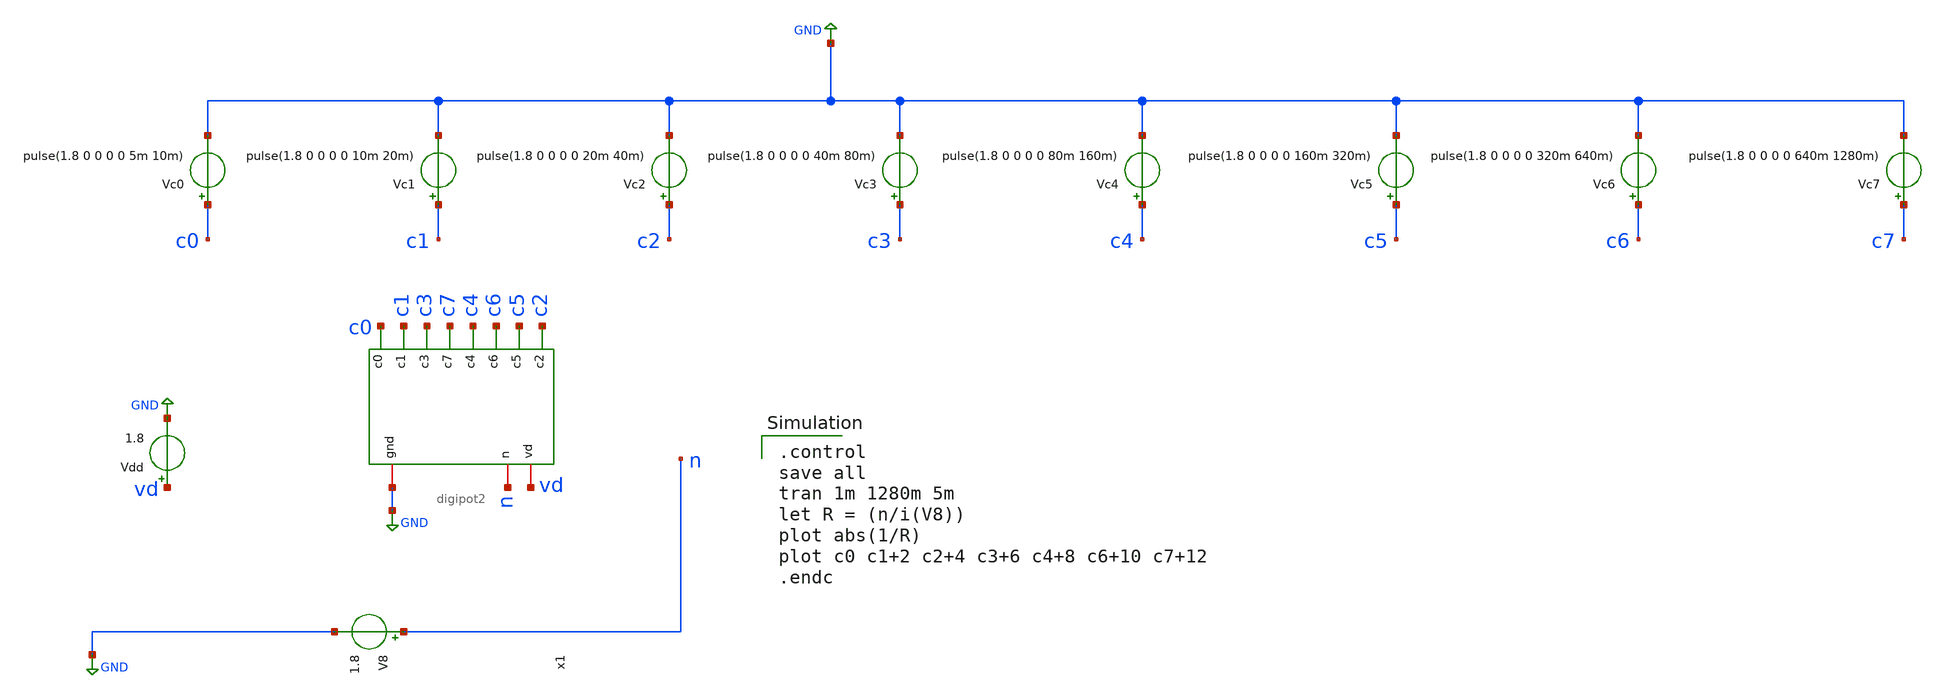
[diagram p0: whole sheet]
** sch_path: .Trash-1000/files/dp2tb.sch
**.subckt dp2tb
V8 n GND 1.8
Vdd vd GND 1.8
Vc0 c0 GND pulse(1.8 0 0 0 0 5m 10m)
Vc1 c1 GND pulse(1.8 0 0 0 0 10m 20m)
Vc2 c2 GND pulse(1.8 0 0 0 0 20m 40m)
Vc3 c3 GND pulse(1.8 0 0 0 0 40m 80m)
Vc4 c4 GND pulse(1.8 0 0 0 0 80m 160m)
Vc5 c5 GND pulse(1.8 0 0 0 0 160m 320m)
Vc6 c6 GND pulse(1.8 0 0 0 0 320m 640m)
Vc7 c7 GND pulse(1.8 0 0 0 0 640m 1280m)
x1 GND vd n c2 c5 c6 c4 c7 c3 c1 c0
**** begin user architecture code

.control
save all
tran 1m 1280m 5m
let R = (n/i(V8))
plot abs(1/R)
plot c0 c1+2 c2+4 c3+6 c4+8 c6+10 c7+12
.endc


** opencircuitdesign pdks install
.lib $::SKYWATER_MODELS/sky130.lib.spice tt_mm


**** end user architecture code
**.ends

* expanding   symbol:  /foss/designs/digipot2.sym # of pins=11
** sym_path: .Trash-1000/files/digipot2.sym
** sch_path: .Trash-1000/files/digipot2.sch
.subckt digipot2 gnd vd n c2 c5 c6 c4 c7 c3 c1 c0 dpideal
*.ipin c0
*.ipin c1
*.ipin c2
*.ipin c3
*.ipin c4
*.ipin c5
*.ipin c6
*.ipin c7
*.iopin gnd
*.iopin vd
*.iopin n
x1 vd c0 gnd net1 gnd tg
x2 vd c1 gnd net2 gnd tg
x3 vd c2 gnd net3 gnd tg
x4 vd c3 gnd net4 gnd tg
x5 vd c4 gnd net5 gnd tg
x6 vd c5 gnd net6 gnd tg
x7 vd c6 gnd net7 gnd tg
x8 vd c7 gnd net8 gnd tg
R1 n net8 3k m=1
R9 n net7 6k m=1
R10 n net6 12k m=1
R11 n net5 24k m=1
R12 n net4 48k m=1
R13 n net2 192k m=1
R14 n net3 96k m=1
R15 n net1 384k m=1
.ends


* expanding   symbol:  /foss/designs/tg.sym # of pins=5
** sym_path: xschem/tg.sym
** sch_path: xschem/tg.sch
.subckt tg vd ctrl vgnd A B
*.iopin B
*.iopin A
*.iopin vgnd
*.iopin vd
*.ipin ctrl
x1 vd ctrl nctrl vgnd inverter
XM1 A ctrl B vgnd sky130_fd_pr__nfet_01v8 L=0.15 W=10 nf=1 ad='int((nf+1)/2) * W/nf * 0.29' as='int((nf+2)/2) * W/nf * 0.29'
+ pd='2*int((nf+1)/2) * (W/nf + 0.29)' ps='2*int((nf+2)/2) * (W/nf + 0.29)' nrd='0.29 / W' nrs='0.29 / W'
+ sa=0 sb=0 sd=0 mult=1 m=1
XM2 A nctrl B vd sky130_fd_pr__pfet_01v8 L=0.15 W=30 nf=1 ad='int((nf+1)/2) * W/nf * 0.29' as='int((nf+2)/2) * W/nf * 0.29'
+ pd='2*int((nf+1)/2) * (W/nf + 0.29)' ps='2*int((nf+2)/2) * (W/nf + 0.29)' nrd='0.29 / W' nrs='0.29 / W'
+ sa=0 sb=0 sd=0 mult=1 m=1
.ends


* expanding   symbol:  /foss/designs/inverter/xschem_files/inverter.sym # of pins=4
** sym_path: /foss/designs/inverter/xschem_files/inverter.sym
** sch_path: /foss/designs/inverter/xschem_files/inverter.sch
.subckt inverter vd in out gnd
*.ipin in
*.opin out
*.iopin vd
*.iopin gnd
XN0 out in gnd gnd sky130_fd_pr__nfet_01v8 L=0.15 W=1 nf=1 ad='int((nf+1)/2) * W/nf * 0.29' as='int((nf+2)/2) * W/nf * 0.29'
+ pd='2*int((nf+1)/2) * (W/nf + 0.29)' ps='2*int((nf+2)/2) * (W/nf + 0.29)' nrd='0.29 / W' nrs='0.29 / W'
+ sa=0 sb=0 sd=0 mult=1 m=1
XP0 out in vd vd sky130_fd_pr__pfet_01v8 L=0.15 W=3 nf=1 ad='int((nf+1)/2) * W/nf * 0.29' as='int((nf+2)/2) * W/nf * 0.29'
+ pd='2*int((nf+1)/2) * (W/nf + 0.29)' ps='2*int((nf+2)/2) * (W/nf + 0.29)' nrd='0.29 / W' nrs='0.29 / W'
+ sa=0 sb=0 sd=0 mult=1 m=1
.ends

.GLOBAL GND
.end
